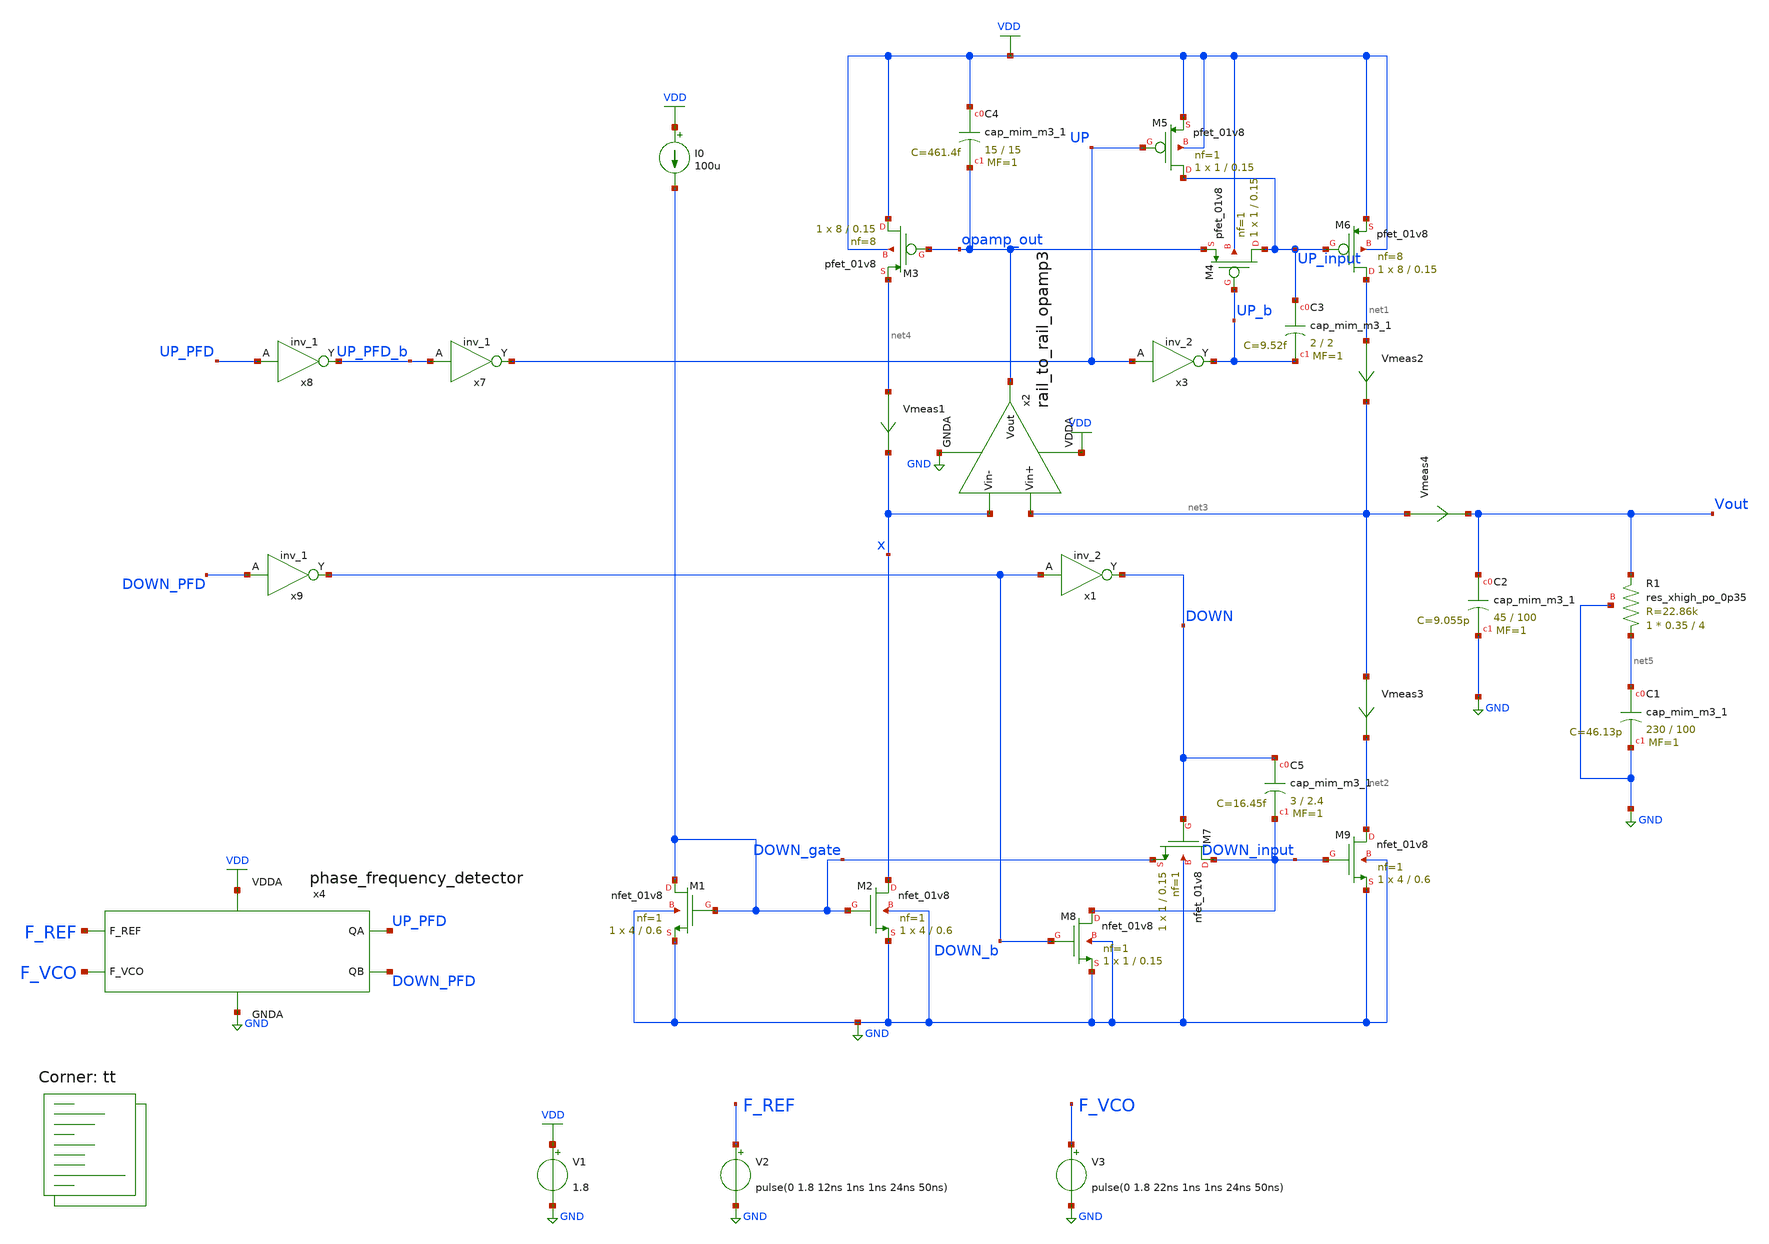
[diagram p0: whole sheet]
** sch_path: projects/pll/charge_pump/xschem_ngspice/pfd_charge_pump.sch
**.subckt pfd_charge_pump
XM1 DOWN_gate DOWN_gate GND GND sky130_fd_pr__nfet_01v8 L=0.6 W=4 nf=1 ad='int((nf+1)/2) * W/nf * 0.29'
+ as='int((nf+2)/2) * W/nf * 0.29' pd='2*int((nf+1)/2) * (W/nf + 0.29)' ps='2*int((nf+2)/2) * (W/nf + 0.29)'
+ nrd='0.29 / W' nrs='0.29 / W' sa=0 sb=0 sd=0 mult=1 m=1
XM2 x DOWN_gate GND GND sky130_fd_pr__nfet_01v8 L=0.6 W=4 nf=1 ad='int((nf+1)/2) * W/nf * 0.29' as='int((nf+2)/2) * W/nf * 0.29'
+ pd='2*int((nf+1)/2) * (W/nf + 0.29)' ps='2*int((nf+2)/2) * (W/nf + 0.29)' nrd='0.29 / W' nrs='0.29 / W'
+ sa=0 sb=0 sd=0 mult=1 m=1
XM3 VDD opamp_out net4 VDD sky130_fd_pr__pfet_01v8 L=0.15 W=8 nf=8 ad='int((nf+1)/2) * W/nf * 0.29' as='int((nf+2)/2) * W/nf * 0.29'
+ pd='2*int((nf+1)/2) * (W/nf + 0.29)' ps='2*int((nf+2)/2) * (W/nf + 0.29)' nrd='0.29 / W' nrs='0.29 / W'
+ sa=0 sb=0 sd=0 mult=1 m=1
V1 VDD GND 1.8
I0 VDD DOWN_gate 100u
Vmeas1 net4 x 0
.save i(vmeas1)
XM4 UP_input UP_b opamp_out VDD sky130_fd_pr__pfet_01v8 L=0.15 W=1 nf=1 ad='int((nf+1)/2) * W/nf * 0.29'
+ as='int((nf+2)/2) * W/nf * 0.29' pd='2*int((nf+1)/2) * (W/nf + 0.29)' ps='2*int((nf+2)/2) * (W/nf + 0.29)'
+ nrd='0.29 / W' nrs='0.29 / W' sa=0 sb=0 sd=0 mult=1 m=1
XM5 UP_input UP VDD VDD sky130_fd_pr__pfet_01v8 L=0.15 W=1 nf=1 ad='int((nf+1)/2) * W/nf * 0.29' as='int((nf+2)/2) * W/nf * 0.29'
+ pd='2*int((nf+1)/2) * (W/nf + 0.29)' ps='2*int((nf+2)/2) * (W/nf + 0.29)' nrd='0.29 / W' nrs='0.29 / W'
+ sa=0 sb=0 sd=0 mult=1 m=1
XM6 net1 UP_input VDD VDD sky130_fd_pr__pfet_01v8 L=0.15 W=8 nf=8 ad='int((nf+1)/2) * W/nf * 0.29' as='int((nf+2)/2) * W/nf * 0.29'
+ pd='2*int((nf+1)/2) * (W/nf + 0.29)' ps='2*int((nf+2)/2) * (W/nf + 0.29)' nrd='0.29 / W' nrs='0.29 / W'
+ sa=0 sb=0 sd=0 mult=1 m=1
Vmeas2 net1 net3 0
.save i(vmeas2)
XM7 DOWN_input DOWN DOWN_gate GND sky130_fd_pr__nfet_01v8 L=0.15 W=1 nf=1 ad='int((nf+1)/2) * W/nf * 0.29'
+ as='int((nf+2)/2) * W/nf * 0.29' pd='2*int((nf+1)/2) * (W/nf + 0.29)' ps='2*int((nf+2)/2) * (W/nf + 0.29)'
+ nrd='0.29 / W' nrs='0.29 / W' sa=0 sb=0 sd=0 mult=1 m=1
XM8 DOWN_input DOWN_b GND GND sky130_fd_pr__nfet_01v8 L=0.15 W=1 nf=1 ad='int((nf+1)/2) * W/nf * 0.29'
+ as='int((nf+2)/2) * W/nf * 0.29' pd='2*int((nf+1)/2) * (W/nf + 0.29)' ps='2*int((nf+2)/2) * (W/nf + 0.29)'
+ nrd='0.29 / W' nrs='0.29 / W' sa=0 sb=0 sd=0 mult=1 m=1
Vmeas3 net3 net2 0
.save i(vmeas3)
XM9 net2 DOWN_input GND GND sky130_fd_pr__nfet_01v8 L=0.6 W=4 nf=1 ad='int((nf+1)/2) * W/nf * 0.29' as='int((nf+2)/2) * W/nf * 0.29'
+ pd='2*int((nf+1)/2) * (W/nf + 0.29)' ps='2*int((nf+2)/2) * (W/nf + 0.29)' nrd='0.29 / W' nrs='0.29 / W'
+ sa=0 sb=0 sd=0 mult=1 m=1
x7 UP_PFD_b GND GND VDD VDD UP sky130_fd_sc_hd__inv_1
x8 UP_PFD GND GND VDD VDD UP_PFD_b sky130_fd_sc_hd__inv_1
x9 DOWN_PFD GND GND VDD VDD DOWN_b sky130_fd_sc_hd__inv_1
x3 UP GND GND VDD VDD UP_b sky130_fd_sc_hd__inv_2
x1 DOWN_b GND GND VDD VDD DOWN sky130_fd_sc_hd__inv_2
XC2 Vout GND sky130_fd_pr__cap_mim_m3_1 W=45 L=100 MF=1 m=1
XC1 net5 GND sky130_fd_pr__cap_mim_m3_1 W=230 L=100 MF=1 m=1
V2 F_REF GND pulse(0 1.8 12ns 1ns 1ns 24ns 50ns)
V3 F_VCO GND pulse(0 1.8 22ns 1ns 1ns 24ns 50ns)
x4 F_REF F_VCO VDD UP_PFD DOWN_PFD GND phase_frequency_detector
Vmeas4 net3 Vout 0
.save i(vmeas4)
x2 VDD net3 x opamp_out GND rail_to_rail_opamp3
XC4 VDD opamp_out sky130_fd_pr__cap_mim_m3_1 W=15 L=15 MF=1 m=1
XC3 UP_input UP_b sky130_fd_pr__cap_mim_m3_1 W=2 L=2 MF=1 m=1
XC5 DOWN DOWN_input sky130_fd_pr__cap_mim_m3_1 W=3 L=2.4 MF=1 m=1
XR1 net5 Vout GND sky130_fd_pr__res_xhigh_po_0p35 L=4 mult=1 m=1
**** begin user architecture code
.lib $::SKYWATER_MODELS/sky130.lib.spice tt



.include /foss/pdks/sky130A/libs.ref/sky130_fd_sc_hd/spice/sky130_fd_sc_hd.spice

.option method=gear trtol1
.option wnflag=1
* .option savecurrents

* .temp = 75

.ic v(vout) = 1.2

.save  v(up_pfd) v(down_pfd) v(up_pfd_b) v(down_pfd_b) v(up) v(up_b) v(down) v(down_b) v(v2) v(x) v(y) v(z) v(vout) v(up_input) v(down_input) v(down_gate) v(opamp_out) v(x2.p_bias) v(x2.n_bias) v(x2.v_common_p) v(x2.v_common_n) v(x2.p_left) v(x2.p_right) v(x2.n_left) v(x2.n_right) v(f_ref) v(f_vco) v(x4.qa) v(x4.qa_b) v(x4.qb) v(x4.qb_b) v(x4.qa) v(x4.e) v(x4.e_b) v(x4.f) v(x4.f_b) v(x4.before_reset) v(x4.reset)


.control
  * save v(up_pfd) v(down_pfd) v(up_pfd_b) v(down_pfd_b) v(up) v(up_b) v(down) v(down_b) v(x)
+ v(vout) v(up_input) v(down_input)
  * save all

  tran 0.1ns 1us
  * dc v2 0 1.8 0.01
  remzerovec
  write pfd_charge_pump.raw
  * wrdata /foss/designs/my_design/projects/pll/charge_pump/xschem_ngspice/charge_pump2_QA.txt
+ v(osc)
  set appendwrite

.endc






**** end user architecture code
**.ends

* expanding   symbol:
*+  /foss/designs/my_design/projects/pll/pfd/xschem_ngspice/phase_frequency_detector.sym # of pins=6
** sym_path: projects/pll/pfd/xschem_ngspice/phase_frequency_detector.sym
** sch_path: projects/pll/pfd/xschem_ngspice/phase_frequency_detector.sch
.subckt phase_frequency_detector F_REF F_VCO VDDA QA QB GNDA
*.ipin F_REF
*.opin QA
*.ipin F_VCO
*.opin QB
*.ipin VDDA
*.ipin GNDA
x1 F_REF QA GNDA GNDA VDDA VDDA QA_b sky130_fd_sc_hd__nor2_1
x2 QA_b E GNDA GNDA VDDA VDDA QA sky130_fd_sc_hd__nor2_1
x3 QA_b E_b GNDA GNDA VDDA VDDA E sky130_fd_sc_hd__nor2_1
x4 E Reset GNDA GNDA VDDA VDDA E_b sky130_fd_sc_hd__nor2_1
x5 F_VCO QB GNDA GNDA VDDA VDDA QB_b sky130_fd_sc_hd__nor2_1
x6 QB_b F GNDA GNDA VDDA VDDA QB sky130_fd_sc_hd__nor2_1
x7 QB_b F_b GNDA GNDA VDDA VDDA F sky130_fd_sc_hd__nor2_1
x8 F Reset GNDA GNDA VDDA VDDA F_b sky130_fd_sc_hd__nor2_1
x9 QA QB GNDA GNDA VDDA VDDA before_Reset sky130_fd_sc_hd__nand2_1
x10 before_Reset GNDA GNDA VDDA VDDA net1 sky130_fd_sc_hd__inv_1
x11 net1 GNDA GNDA VDDA VDDA net2 sky130_fd_sc_hd__inv_1
x12 net2 GNDA GNDA VDDA VDDA net3 sky130_fd_sc_hd__inv_1
x13 net3 GNDA GNDA VDDA VDDA net4 sky130_fd_sc_hd__inv_1
x14 net4 GNDA GNDA VDDA VDDA Reset sky130_fd_sc_hd__inv_1
.ends


* expanding   symbol:
*+  /foss/designs/my_design/projects/pll/charge_pump/xschem_ngspice/rail_to_rail_opamp3.sym # of pins=5
** sym_path: projects/pll/charge_pump/xschem_ngspice/rail_to_rail_opamp3.sym
** sch_path: projects/pll/charge_pump/xschem_ngspice/rail_to_rail_opamp3.sch
.subckt rail_to_rail_opamp3 VDDA Vin+ Vin- Vout GNDA
*.opin Vout
*.ipin Vin+
*.ipin Vin-
*.ipin VDDA
*.ipin GNDA
XM2 n_left Vin+ v_common_n GNDA sky130_fd_pr__nfet_01v8 L=0.15 W=1 nf=1 ad='int((nf+1)/2) * W/nf * 0.29'
+ as='int((nf+2)/2) * W/nf * 0.29' pd='2*int((nf+1)/2) * (W/nf + 0.29)' ps='2*int((nf+2)/2) * (W/nf + 0.29)'
+ nrd='0.29 / W' nrs='0.29 / W' sa=0 sb=0 sd=0 mult=1 m=1
XM3 n_right Vin- v_common_n GNDA sky130_fd_pr__nfet_01v8 L=0.15 W=1 nf=1 ad='int((nf+1)/2) * W/nf * 0.29'
+ as='int((nf+2)/2) * W/nf * 0.29' pd='2*int((nf+1)/2) * (W/nf + 0.29)' ps='2*int((nf+2)/2) * (W/nf + 0.29)'
+ nrd='0.29 / W' nrs='0.29 / W' sa=0 sb=0 sd=0 mult=1 m=1
XM5 n_left n_left VDDA VDDA sky130_fd_pr__pfet_01v8 L=0.15 W=2 nf=2 ad='int((nf+1)/2) * W/nf * 0.29'
+ as='int((nf+2)/2) * W/nf * 0.29' pd='2*int((nf+1)/2) * (W/nf + 0.29)' ps='2*int((nf+2)/2) * (W/nf + 0.29)'
+ nrd='0.29 / W' nrs='0.29 / W' sa=0 sb=0 sd=0 mult=1 m=1
XM4 n_right n_left VDDA VDDA sky130_fd_pr__pfet_01v8 L=0.15 W=2 nf=2 ad='int((nf+1)/2) * W/nf * 0.29'
+ as='int((nf+2)/2) * W/nf * 0.29' pd='2*int((nf+1)/2) * (W/nf + 0.29)' ps='2*int((nf+2)/2) * (W/nf + 0.29)'
+ nrd='0.29 / W' nrs='0.29 / W' sa=0 sb=0 sd=0 mult=1 m=1
XM6 v_common_p p_bias VDDA VDDA sky130_fd_pr__pfet_01v8 L=0.15 W=3 nf=3 ad='int((nf+1)/2) * W/nf * 0.29'
+ as='int((nf+2)/2) * W/nf * 0.29' pd='2*int((nf+1)/2) * (W/nf + 0.29)' ps='2*int((nf+2)/2) * (W/nf + 0.29)'
+ nrd='0.29 / W' nrs='0.29 / W' sa=0 sb=0 sd=0 mult=1 m=1
XM7 p_left Vin+ v_common_p VDDA sky130_fd_pr__pfet_01v8 L=0.15 W=2 nf=2 ad='int((nf+1)/2) * W/nf * 0.29'
+ as='int((nf+2)/2) * W/nf * 0.29' pd='2*int((nf+1)/2) * (W/nf + 0.29)' ps='2*int((nf+2)/2) * (W/nf + 0.29)'
+ nrd='0.29 / W' nrs='0.29 / W' sa=0 sb=0 sd=0 mult=1 m=1
XM8 p_right Vin- v_common_p VDDA sky130_fd_pr__pfet_01v8 L=0.15 W=2 nf=2 ad='int((nf+1)/2) * W/nf * 0.29'
+ as='int((nf+2)/2) * W/nf * 0.29' pd='2*int((nf+1)/2) * (W/nf + 0.29)' ps='2*int((nf+2)/2) * (W/nf + 0.29)'
+ nrd='0.29 / W' nrs='0.29 / W' sa=0 sb=0 sd=0 mult=1 m=1
XM9 p_left p_left GNDA GNDA sky130_fd_pr__nfet_01v8 L=0.15 W=1 nf=1 ad='int((nf+1)/2) * W/nf * 0.29'
+ as='int((nf+2)/2) * W/nf * 0.29' pd='2*int((nf+1)/2) * (W/nf + 0.29)' ps='2*int((nf+2)/2) * (W/nf + 0.29)'
+ nrd='0.29 / W' nrs='0.29 / W' sa=0 sb=0 sd=0 mult=1 m=1
XM10 p_right p_left GNDA GNDA sky130_fd_pr__nfet_01v8 L=0.15 W=1 nf=1 ad='int((nf+1)/2) * W/nf * 0.29'
+ as='int((nf+2)/2) * W/nf * 0.29' pd='2*int((nf+1)/2) * (W/nf + 0.29)' ps='2*int((nf+2)/2) * (W/nf + 0.29)'
+ nrd='0.29 / W' nrs='0.29 / W' sa=0 sb=0 sd=0 mult=1 m=1
XM1 v_common_n n_bias GNDA GNDA sky130_fd_pr__nfet_01v8 L=0.15 W=1 nf=1 ad='int((nf+1)/2) * W/nf * 0.29'
+ as='int((nf+2)/2) * W/nf * 0.29' pd='2*int((nf+1)/2) * (W/nf + 0.29)' ps='2*int((nf+2)/2) * (W/nf + 0.29)'
+ nrd='0.29 / W' nrs='0.29 / W' sa=0 sb=0 sd=0 mult=1 m=1
XM11 Vout n_right VDDA VDDA sky130_fd_pr__pfet_01v8 L=0.15 W=16 nf=2 ad='int((nf+1)/2) * W/nf * 0.29'
+ as='int((nf+2)/2) * W/nf * 0.29' pd='2*int((nf+1)/2) * (W/nf + 0.29)' ps='2*int((nf+2)/2) * (W/nf + 0.29)'
+ nrd='0.29 / W' nrs='0.29 / W' sa=0 sb=0 sd=0 mult=1 m=1
XM12 Vout p_right GNDA GNDA sky130_fd_pr__nfet_01v8 L=0.15 W=8 nf=1 ad='int((nf+1)/2) * W/nf * 0.29'
+ as='int((nf+2)/2) * W/nf * 0.29' pd='2*int((nf+1)/2) * (W/nf + 0.29)' ps='2*int((nf+2)/2) * (W/nf + 0.29)'
+ nrd='0.29 / W' nrs='0.29 / W' sa=0 sb=0 sd=0 mult=1 m=1
XM13 n_bias n_bias GNDA GNDA sky130_fd_pr__nfet_01v8 L=0.15 W=1 nf=1 ad='int((nf+1)/2) * W/nf * 0.29'
+ as='int((nf+2)/2) * W/nf * 0.29' pd='2*int((nf+1)/2) * (W/nf + 0.29)' ps='2*int((nf+2)/2) * (W/nf + 0.29)'
+ nrd='0.29 / W' nrs='0.29 / W' sa=0 sb=0 sd=0 mult=1 m=1
XM15 p_bias p_bias VDDA VDDA sky130_fd_pr__pfet_01v8 L=0.15 W=2 nf=2 ad='int((nf+1)/2) * W/nf * 0.29'
+ as='int((nf+2)/2) * W/nf * 0.29' pd='2*int((nf+1)/2) * (W/nf + 0.29)' ps='2*int((nf+2)/2) * (W/nf + 0.29)'
+ nrd='0.29 / W' nrs='0.29 / W' sa=0 sb=0 sd=0 mult=1 m=1
Vmeas net1 n_bias 0
.save i(vmeas)
XM14 net1 net1 p_bias p_bias sky130_fd_pr__pfet_01v8 L=0.15 W=2 nf=2 ad='int((nf+1)/2) * W/nf * 0.29'
+ as='int((nf+2)/2) * W/nf * 0.29' pd='2*int((nf+1)/2) * (W/nf + 0.29)' ps='2*int((nf+2)/2) * (W/nf + 0.29)'
+ nrd='0.29 / W' nrs='0.29 / W' sa=0 sb=0 sd=0 mult=1 m=1
.ends

.GLOBAL VDD
.GLOBAL GND
.end
